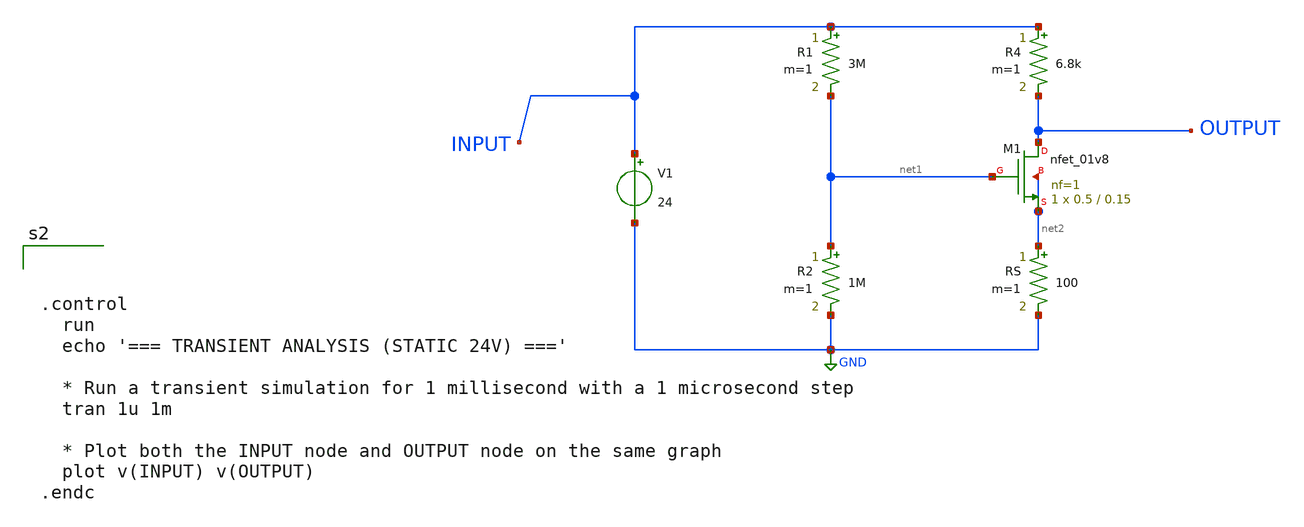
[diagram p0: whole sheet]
** sch_path: cmosvoltagedivider.sch
**.subckt cmosvoltagedivider
XM1 OUTPUT net1 net2 net2 sky130_fd_pr__nfet_01v8 L=0.15 W=0.5 nf=1 ad='int((1 + 1)/2) * 0.5 / 1 * 0.29'
+ as='int((1 + 2)/2) * 0.5 / 1 * 0.29' pd='2*int((1 + 1)/2) * (0.5 / 1 + 0.29)' ps='2*int((1 + 2)/2) * (0.5 / 1 + 0.29)'
+ nrd='0.29 / 0.5 ' nrs='0.29 / 0.5 ' sa=0 sb=0 sd=0 mult=1 m=1
R1 INPUT net1 3M m=1
R2 net1 GND 1M m=1
RS net2 GND 100 m=1
R4 INPUT OUTPUT 6.8k m=1
V1 INPUT GND 24
**** begin user architecture code



.lib /foss/pdks/sky130A/libs.tech/ngspice/sky130.lib.spice tt

* Discrete JFET Model for the Voltage Divider Circuit
.model jfet_n njf(beta=1m vto=-2.0)
.op





.control
  run
  echo '=== TRANSIENT ANALYSIS (STATIC 24V) ==='

  * Run a transient simulation for 1 millisecond with a 1 microsecond step
  tran 1u 1m

  * Plot both the INPUT node and OUTPUT node on the same graph
  plot v(INPUT) v(OUTPUT)
.endc


**** end user architecture code
**.ends
.GLOBAL GND
.end
